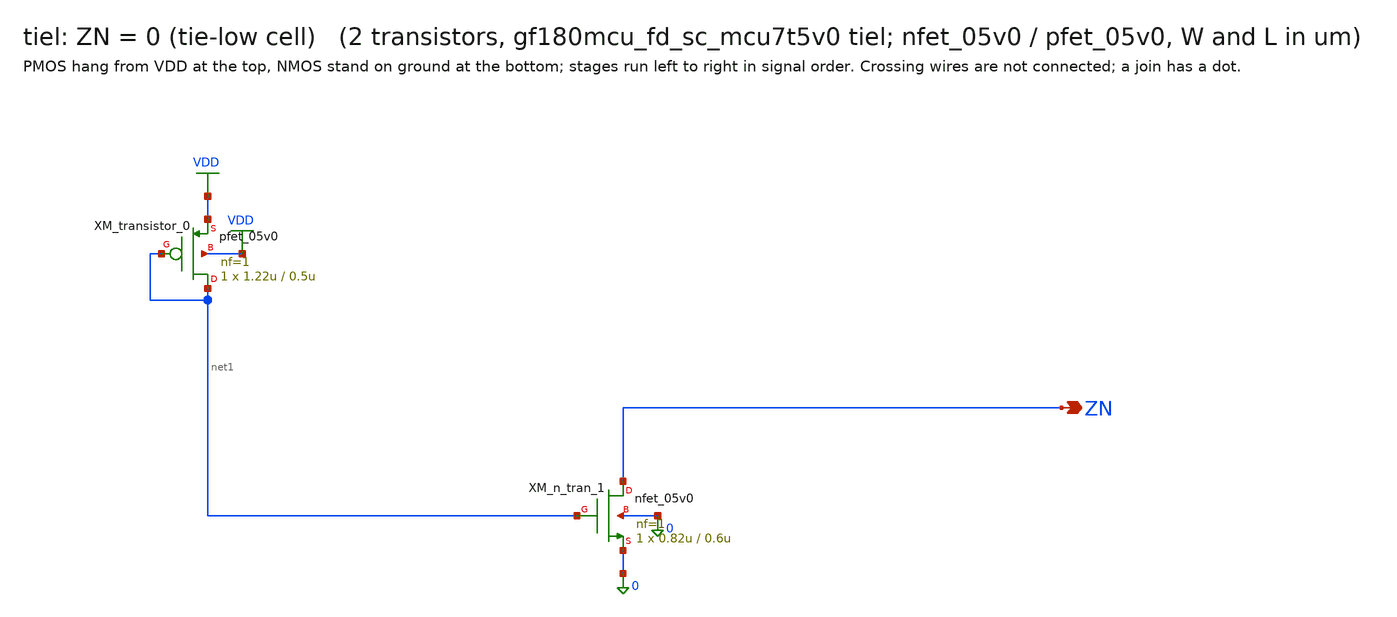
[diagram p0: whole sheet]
** sch_path: xschem/cells_tx/tiel.sch
**.subckt tiel ZN
*.opin ZN
XM_n_tran_1 ZN net1 0 0 nfet_05v0 L=0.6u W=0.82u nf=1 ad=4.1e-13 as=4.1e-13 pd=2.64e-06 ps=2.64e-06
+ nrd=0 nrs=0 sa=0 sb=0 sd=0 m=1
XM_transistor_0 net1 net1 VDD VDD pfet_05v0 L=0.5u W=1.22u nf=1 ad=6.1e-13 as=6.1e-13 pd=3.44e-06
+ ps=3.44e-06 nrd=0 nrs=0 sa=0 sb=0 sd=0 m=1
**.ends
.GLOBAL VDD
.end
